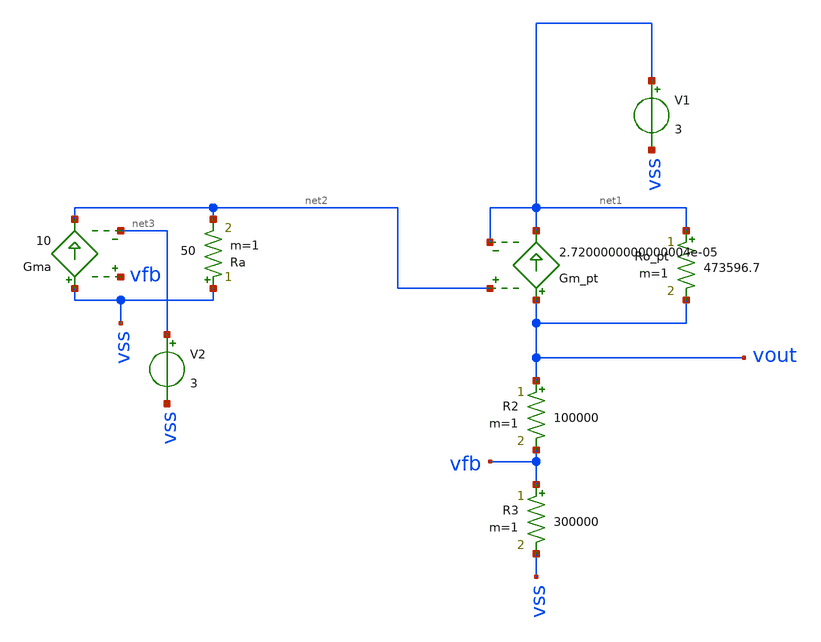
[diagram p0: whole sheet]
** sch_path: test/sstadex/xschem/ldo.sch
**.subckt ldo
Ro_pt net1 vout 473596.7 m=1
Gm_pt vout net1 net2 net1 2.7200000000000004e-05
R2 vout vfb 100000 m=1
R3 vfb vss 300000 m=1
Gma vss net2 vfb net3 10
Ra vss net2 50 m=1
V1 net1 vss 3
V2 net3 vss 3
**.ends
.end
